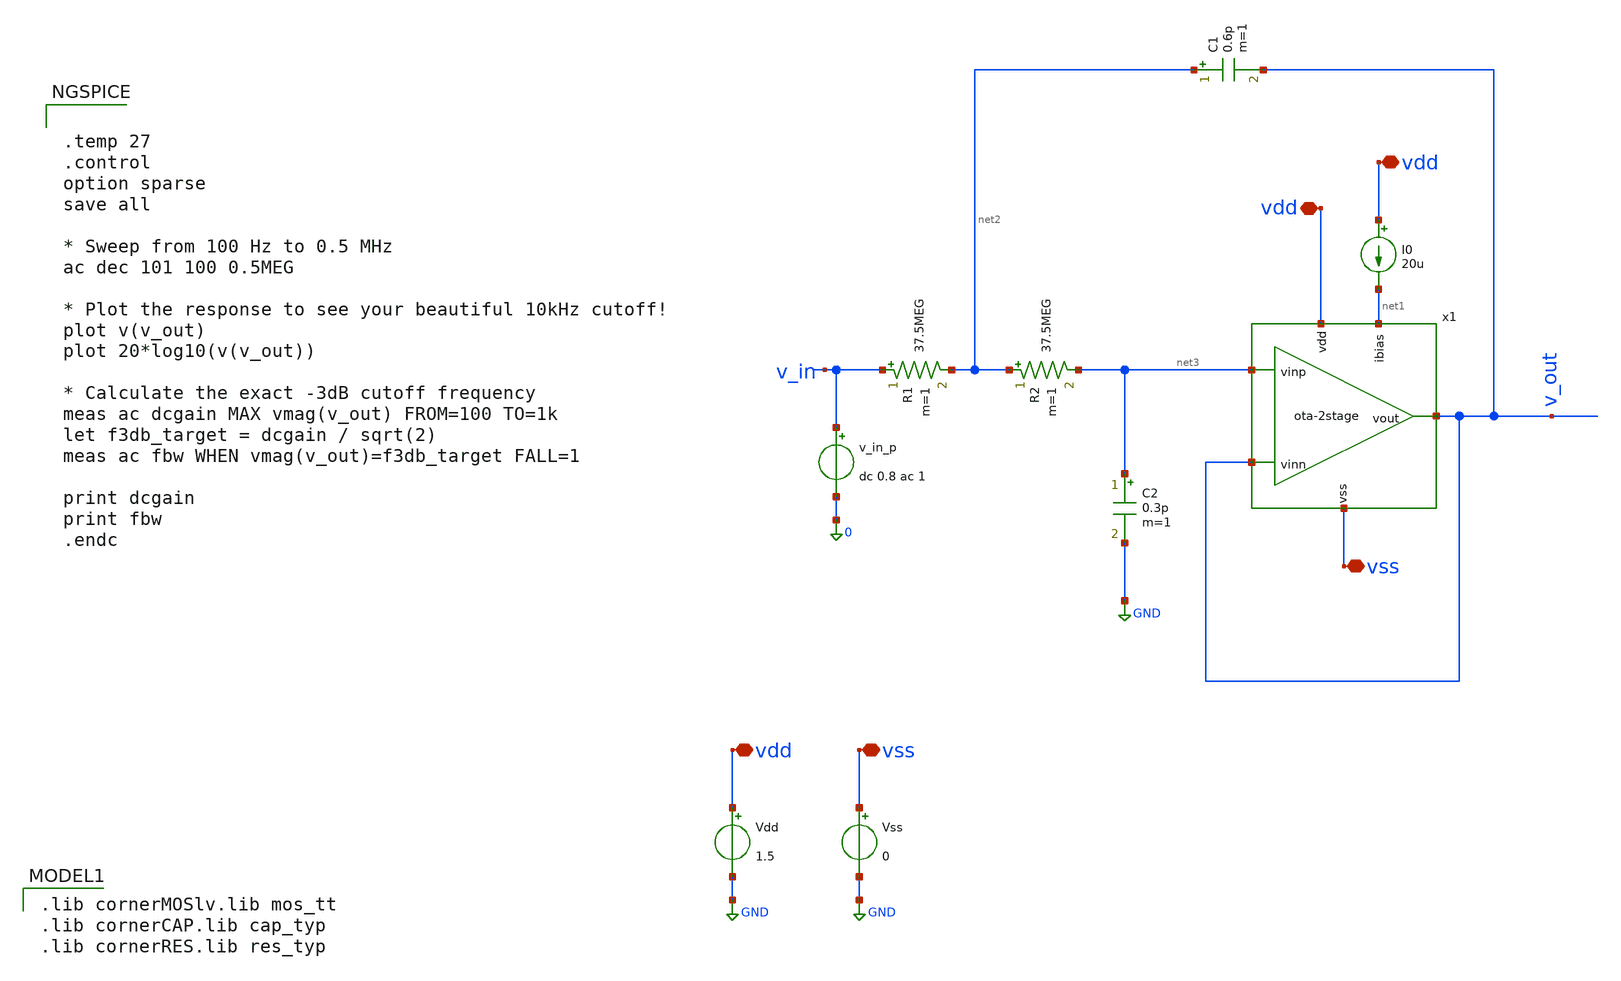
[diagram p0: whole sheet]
** sch_path: Testbench/ota-2stage_tb-sk-lpf.sch
**.subckt ota-2stage_tb-sk-lpf vdd vdd vdd vss vss
*.iopin vdd
*.iopin vdd
*.iopin vdd
*.iopin vss
*.iopin vss
I0 vdd net1 20u
Vdd vdd GND 1.5
Vss vss GND 0
v_in_p v_in 0 dc 0.8 ac 1
R1 v_in net2 37.5MEG m=1
R2 net2 net3 37.5MEG m=1
C2 net3 GND 0.3p m=1
C1 net2 v_out 0.6p m=1
x1 vdd net1 v_out v_out net3 vss ota-2stage
**** begin user architecture code


.temp 27
.control
option sparse
save all

* Sweep from 100 Hz to 0.5 MHz
ac dec 101 100 0.5MEG

* Plot the response to see your beautiful 10kHz cutoff!
plot v(v_out)
plot 20*log10(v(v_out))

* Calculate the exact -3dB cutoff frequency
meas ac dcgain MAX vmag(v_out) FROM=100 TO=1k
let f3db_target = dcgain / sqrt(2)
meas ac fbw WHEN vmag(v_out)=f3db_target FALL=1

print dcgain
print fbw
.endc


 .lib cornerMOSlv.lib mos_tt
.lib cornerCAP.lib cap_typ
.lib cornerRES.lib res_typ

**** end user architecture code
**.ends

* expanding   symbol:  ota-2stage.sym # of pins=6
** sym_path: Testbench/ota-2stage.sym
** sch_path: Testbench/ota-2stage.sch
.subckt ota-2stage vdd ibias vinn vout vinp vss
*.iopin vdd
*.iopin vss
*.ipin ibias
*.ipin vout
*.ipin vinn
*.ipin vinp
XM1 net1 vinn net3 net3 sg13_lv_nmos w=2u l=5u ng=1 m=1 mm_ok=1
XM2 net2 vinp net3 net3 sg13_lv_nmos w=2u l=5u ng=1 m=1 mm_ok=1
XM4 net2 net1 vdd vdd sg13_lv_pmos w=2.5u l=5u ng=1 m=1 mm_ok=1
XM3 net1 net1 vdd vdd sg13_lv_pmos w=2.5u l=5u ng=1 m=1 mm_ok=1
XM5 vout net2 vdd vdd sg13_lv_pmos w=6.25u l=5u ng=5 m=1 mm_ok=1
XM6 ibias ibias vss vss sg13_lv_nmos w=5u l=5u ng=1 m=1 mm_ok=1
XM7 net3 ibias vss vss sg13_lv_nmos w=1u l=5u ng=1 m=1 mm_ok=1
XM8 vout ibias vss vss sg13_lv_nmos w=6.25u l=5u ng=1 m=1 mm_ok=1
XCM net2 vout cap_cmim w=14.2e-6 l=14.2e-6 m=1 mm_ok=1
.ends

.GLOBAL GND
.end
